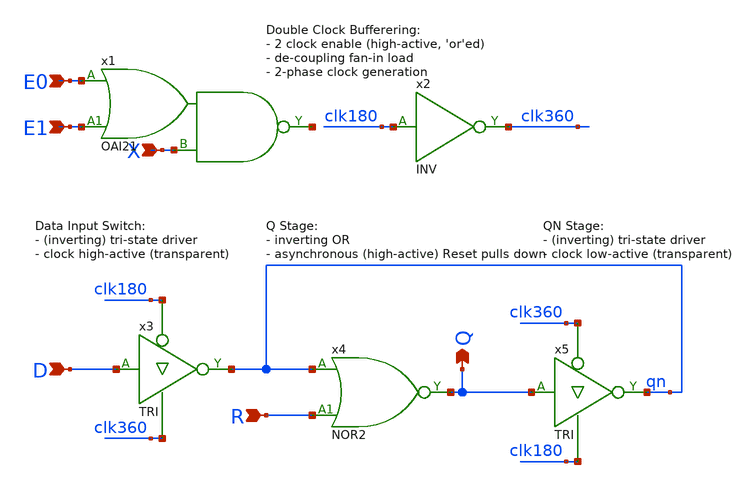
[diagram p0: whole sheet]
** sch_path: Sources/crafted/LATPEER.sch
**.subckt LATPEER X D Q E0 E1 R
*.ipin X
*.ipin D
*.opin Q
*.ipin E0
*.ipin E1
*.ipin R
x1 E0 E1 X net1 VDD GND OAI21 Wmin=1.5u Lmin=1u g=2 m=1
x2 clk180 clk360 VDD GND INV Wmin=1.5u Lmin=1u g=2 m=1
x3 D clk180 clk360 qn VDD GND TRI Wmin=1.5u Lmin=1u g=2 m=1
x5 Q clk360 clk180 qn VDD GND TRI Wmin=1.5u Lmin=1u g=2 m=1
x4 qn R Q VDD GND NOR2 Wmin=1.5u Lmin=1u g=2 m=1
**.ends
.end
